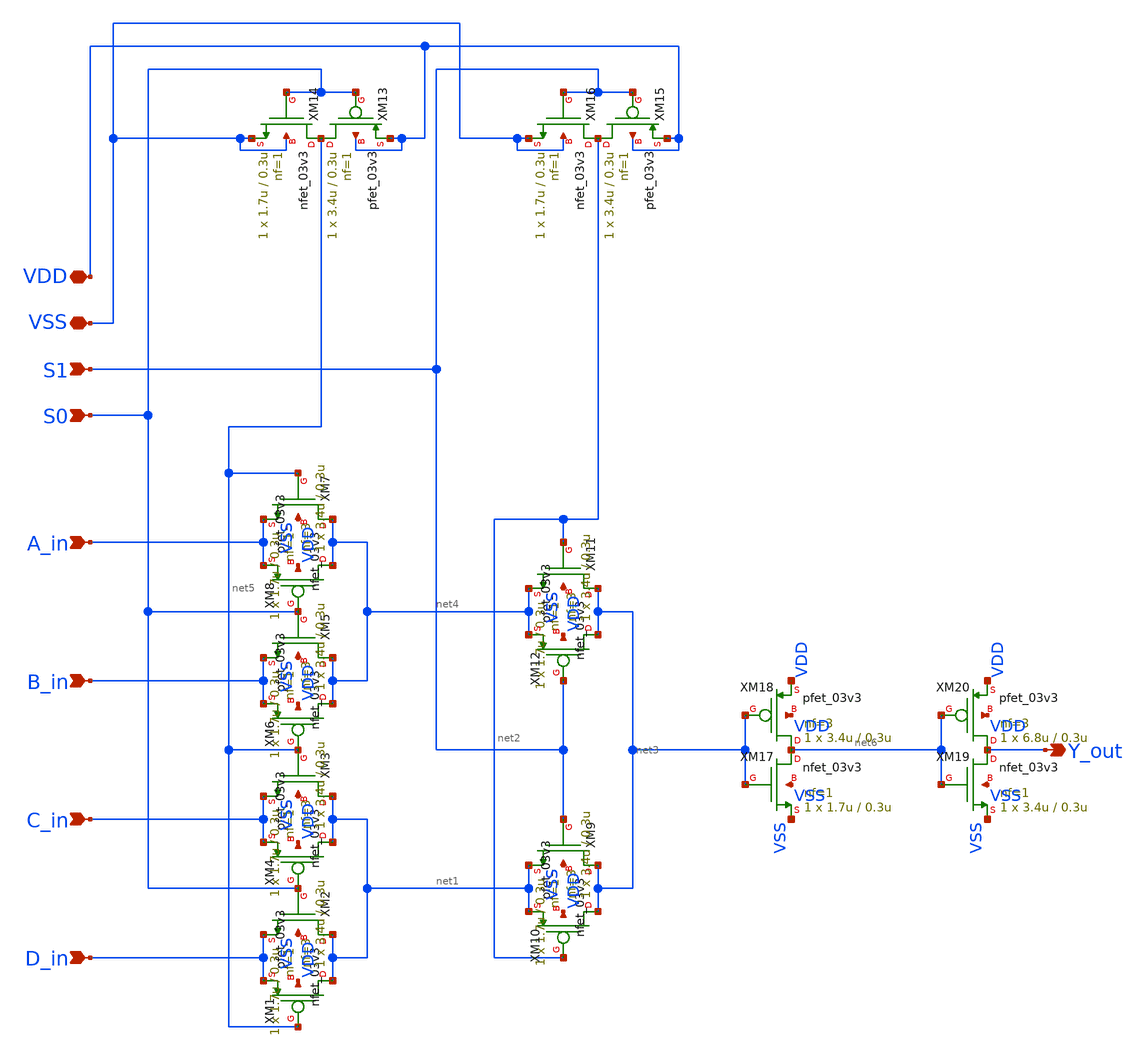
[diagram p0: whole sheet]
** sch_path: MUX41/MUX41PTLBuffer/MUX41PTLBuffer.sch
**.subckt MUX41PTLBuffer D_in C_in B_in A_in S0 S1 VSS VDD Y_out
*.ipin D_in
*.ipin C_in
*.ipin B_in
*.ipin A_in
*.ipin S0
*.ipin S1
*.iopin VSS
*.iopin VDD
*.opin Y_out
XM2 net1 S0 D_in VSS nfet_03v3 L=0.3u W=1.7u nf=1 ad='int((nf+1)/2) * W/nf * 0.18u' as='int((nf+2)/2) * W/nf * 0.18u'
+ pd='2*int((nf+1)/2) * (W/nf + 0.18u)' ps='2*int((nf+2)/2) * (W/nf + 0.18u)' nrd='0.18u / W' nrs='0.18u / W'
+ sa=0 sb=0 sd=0 m=1
XM14 net5 S0 VSS VSS nfet_03v3 L=0.3u W=1.7u nf=1 ad='int((nf+1)/2) * W/nf * 0.18u' as='int((nf+2)/2) * W/nf * 0.18u'
+ pd='2*int((nf+1)/2) * (W/nf + 0.18u)' ps='2*int((nf+2)/2) * (W/nf + 0.18u)' nrd='0.18u / W' nrs='0.18u / W'
+ sa=0 sb=0 sd=0 m=1
XM13 net5 S0 VDD VDD pfet_03v3 L=0.3u W=3.4u nf=1 ad='int((nf+1)/2) * W/nf * 0.18u' as='int((nf+2)/2) * W/nf * 0.18u'
+ pd='2*int((nf+1)/2) * (W/nf + 0.18u)' ps='2*int((nf+2)/2) * (W/nf + 0.18u)' nrd='0.18u / W' nrs='0.18u / W'
+ sa=0 sb=0 sd=0 m=1
XM16 net2 S1 VSS VSS nfet_03v3 L=0.3u W=1.7u nf=1 ad='int((nf+1)/2) * W/nf * 0.18u' as='int((nf+2)/2) * W/nf * 0.18u'
+ pd='2*int((nf+1)/2) * (W/nf + 0.18u)' ps='2*int((nf+2)/2) * (W/nf + 0.18u)' nrd='0.18u / W' nrs='0.18u / W'
+ sa=0 sb=0 sd=0 m=1
XM15 net2 S1 VDD VDD pfet_03v3 L=0.3u W=3.4u nf=1 ad='int((nf+1)/2) * W/nf * 0.18u' as='int((nf+2)/2) * W/nf * 0.18u'
+ pd='2*int((nf+1)/2) * (W/nf + 0.18u)' ps='2*int((nf+2)/2) * (W/nf + 0.18u)' nrd='0.18u / W' nrs='0.18u / W'
+ sa=0 sb=0 sd=0 m=1
XM1 net1 net5 D_in VDD pfet_03v3 L=0.3u W=3.4u nf=3 ad='int((nf+1)/2) * W/nf * 0.18u' as='int((nf+2)/2) * W/nf * 0.18u'
+ pd='2*int((nf+1)/2) * (W/nf + 0.18u)' ps='2*int((nf+2)/2) * (W/nf + 0.18u)' nrd='0.18u / W' nrs='0.18u / W'
+ sa=0 sb=0 sd=0 m=1
XM3 net1 net5 C_in VSS nfet_03v3 L=0.3u W=1.7u nf=1 ad='int((nf+1)/2) * W/nf * 0.18u' as='int((nf+2)/2) * W/nf * 0.18u'
+ pd='2*int((nf+1)/2) * (W/nf + 0.18u)' ps='2*int((nf+2)/2) * (W/nf + 0.18u)' nrd='0.18u / W' nrs='0.18u / W'
+ sa=0 sb=0 sd=0 m=1
XM4 net1 S0 C_in VDD pfet_03v3 L=0.3u W=3.4u nf=3 ad='int((nf+1)/2) * W/nf * 0.18u' as='int((nf+2)/2) * W/nf * 0.18u'
+ pd='2*int((nf+1)/2) * (W/nf + 0.18u)' ps='2*int((nf+2)/2) * (W/nf + 0.18u)' nrd='0.18u / W' nrs='0.18u / W'
+ sa=0 sb=0 sd=0 m=1
XM5 net4 S0 B_in VSS nfet_03v3 L=0.3u W=1.7u nf=1 ad='int((nf+1)/2) * W/nf * 0.18u' as='int((nf+2)/2) * W/nf * 0.18u'
+ pd='2*int((nf+1)/2) * (W/nf + 0.18u)' ps='2*int((nf+2)/2) * (W/nf + 0.18u)' nrd='0.18u / W' nrs='0.18u / W'
+ sa=0 sb=0 sd=0 m=1
XM6 net4 net5 B_in VDD pfet_03v3 L=0.3u W=3.4u nf=3 ad='int((nf+1)/2) * W/nf * 0.18u' as='int((nf+2)/2) * W/nf * 0.18u'
+ pd='2*int((nf+1)/2) * (W/nf + 0.18u)' ps='2*int((nf+2)/2) * (W/nf + 0.18u)' nrd='0.18u / W' nrs='0.18u / W'
+ sa=0 sb=0 sd=0 m=1
XM7 net4 net5 A_in VSS nfet_03v3 L=0.3u W=1.7u nf=1 ad='int((nf+1)/2) * W/nf * 0.18u' as='int((nf+2)/2) * W/nf * 0.18u'
+ pd='2*int((nf+1)/2) * (W/nf + 0.18u)' ps='2*int((nf+2)/2) * (W/nf + 0.18u)' nrd='0.18u / W' nrs='0.18u / W'
+ sa=0 sb=0 sd=0 m=1
XM8 net4 S0 A_in VDD pfet_03v3 L=0.3u W=3.4u nf=3 ad='int((nf+1)/2) * W/nf * 0.18u' as='int((nf+2)/2) * W/nf * 0.18u'
+ pd='2*int((nf+1)/2) * (W/nf + 0.18u)' ps='2*int((nf+2)/2) * (W/nf + 0.18u)' nrd='0.18u / W' nrs='0.18u / W'
+ sa=0 sb=0 sd=0 m=1
XM9 net3 S1 net1 VSS nfet_03v3 L=0.3u W=1.7u nf=1 ad='int((nf+1)/2) * W/nf * 0.18u' as='int((nf+2)/2) * W/nf * 0.18u'
+ pd='2*int((nf+1)/2) * (W/nf + 0.18u)' ps='2*int((nf+2)/2) * (W/nf + 0.18u)' nrd='0.18u / W' nrs='0.18u / W'
+ sa=0 sb=0 sd=0 m=1
XM10 net3 net2 net1 VDD pfet_03v3 L=0.3u W=3.4u nf=3 ad='int((nf+1)/2) * W/nf * 0.18u' as='int((nf+2)/2) * W/nf * 0.18u'
+ pd='2*int((nf+1)/2) * (W/nf + 0.18u)' ps='2*int((nf+2)/2) * (W/nf + 0.18u)' nrd='0.18u / W' nrs='0.18u / W'
+ sa=0 sb=0 sd=0 m=1
XM11 net3 net2 net4 VSS nfet_03v3 L=0.3u W=1.7u nf=1 ad='int((nf+1)/2) * W/nf * 0.18u' as='int((nf+2)/2) * W/nf * 0.18u'
+ pd='2*int((nf+1)/2) * (W/nf + 0.18u)' ps='2*int((nf+2)/2) * (W/nf + 0.18u)' nrd='0.18u / W' nrs='0.18u / W'
+ sa=0 sb=0 sd=0 m=1
XM12 net3 S1 net4 VDD pfet_03v3 L=0.3u W=3.4u nf=3 ad='int((nf+1)/2) * W/nf * 0.18u' as='int((nf+2)/2) * W/nf * 0.18u'
+ pd='2*int((nf+1)/2) * (W/nf + 0.18u)' ps='2*int((nf+2)/2) * (W/nf + 0.18u)' nrd='0.18u / W' nrs='0.18u / W'
+ sa=0 sb=0 sd=0 m=1
XM17 net6 net3 VSS VSS nfet_03v3 L=0.3u W=1.7u nf=1 ad='int((nf+1)/2) * W/nf * 0.18u' as='int((nf+2)/2) * W/nf * 0.18u'
+ pd='2*int((nf+1)/2) * (W/nf + 0.18u)' ps='2*int((nf+2)/2) * (W/nf + 0.18u)' nrd='0.18u / W' nrs='0.18u / W'
+ sa=0 sb=0 sd=0 m=1
XM18 net6 net3 VDD VDD pfet_03v3 L=0.3u W=3.4u nf=3 ad='int((nf+1)/2) * W/nf * 0.18u' as='int((nf+2)/2) * W/nf * 0.18u'
+ pd='2*int((nf+1)/2) * (W/nf + 0.18u)' ps='2*int((nf+2)/2) * (W/nf + 0.18u)' nrd='0.18u / W' nrs='0.18u / W'
+ sa=0 sb=0 sd=0 m=1
XM19 Y_out net6 VSS VSS nfet_03v3 L=0.3u W=3.4u nf=1 ad='int((nf+1)/2) * W/nf * 0.18u' as='int((nf+2)/2) * W/nf * 0.18u'
+ pd='2*int((nf+1)/2) * (W/nf + 0.18u)' ps='2*int((nf+2)/2) * (W/nf + 0.18u)' nrd='0.18u / W' nrs='0.18u / W'
+ sa=0 sb=0 sd=0 m=1
XM20 Y_out net6 VDD VDD pfet_03v3 L=0.3u W=6.8u nf=3 ad='int((nf+1)/2) * W/nf * 0.18u' as='int((nf+2)/2) * W/nf * 0.18u'
+ pd='2*int((nf+1)/2) * (W/nf + 0.18u)' ps='2*int((nf+2)/2) * (W/nf + 0.18u)' nrd='0.18u / W' nrs='0.18u / W'
+ sa=0 sb=0 sd=0 m=1
**.ends
.end
